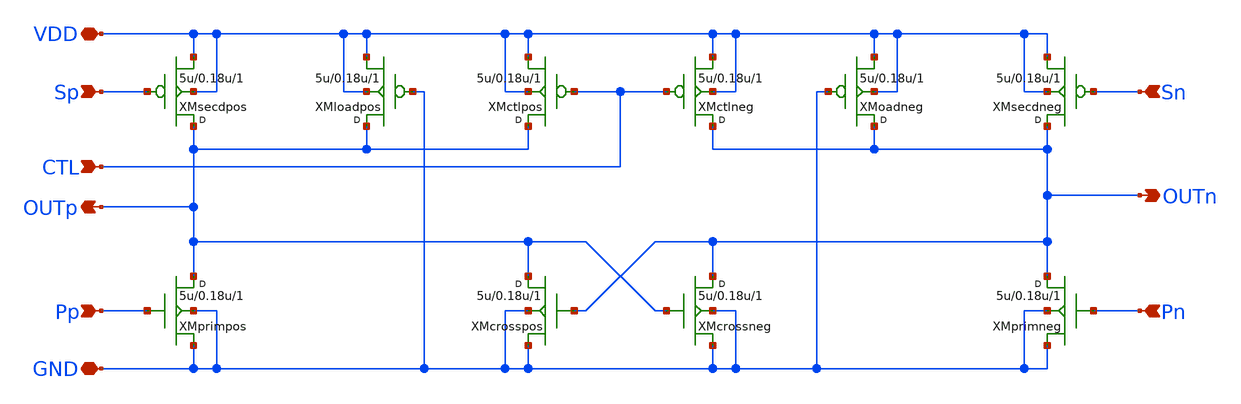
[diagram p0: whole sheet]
** sch_path: design/vco_delaycell_feedforward/vco_delaycell.sch
**.subckt vco_delaycell Pp Pn Sp Sn OUTn OUTp VDD GND CTL
*.ipin Pp
*.ipin Pn
*.ipin Sp
*.ipin Sn
*.opin OUTn
*.opin OUTp
*.iopin VDD
*.iopin GND
*.ipin CTL
XMprimpos OUTp Pp GND GND sky130_fd_pr__rf_nfet_01v8_bM04W5p00L0p15 w=5u l=0.18u m=1
XMcrossneg OUTn OUTp GND GND sky130_fd_pr__rf_nfet_01v8_bM04W5p00L0p15 w=5u l=0.18u m=1
XMctlneg OUTn CTL VDD VDD sky130_fd_pr__rf_pfet_01v8_bM02W1p65L0p25 w=5u l=0.18u m=1
XMctlpos OUTp CTL VDD VDD sky130_fd_pr__rf_pfet_01v8_bM02W1p65L0p25 w=5u l=0.18u m=1
XMloadpos OUTp GND VDD VDD sky130_fd_pr__rf_pfet_01v8_bM02W1p65L0p25 w=5u l=0.18u m=1
XMsecdneg OUTn Sn VDD VDD sky130_fd_pr__rf_pfet_01v8_aF02W0p84L0p15 w=5u l=0.18u m=1
XMsecdpos OUTp Sp VDD VDD sky130_fd_pr__rf_pfet_01v8_aF02W0p84L0p15 w=5u l=0.18u m=1
XMcrosspos OUTp OUTn GND GND sky130_fd_pr__rf_nfet_01v8_bM04W5p00L0p15 w=5u l=0.18u m=1
XMprimneg OUTn Pn GND GND sky130_fd_pr__rf_nfet_01v8_bM04W5p00L0p15 w=5u l=0.18u m=1
XMoadneg OUTn GND VDD VDD sky130_fd_pr__rf_pfet_01v8_bM02W1p65L0p25 w=5u l=0.18u m=1
**.ends
.end
